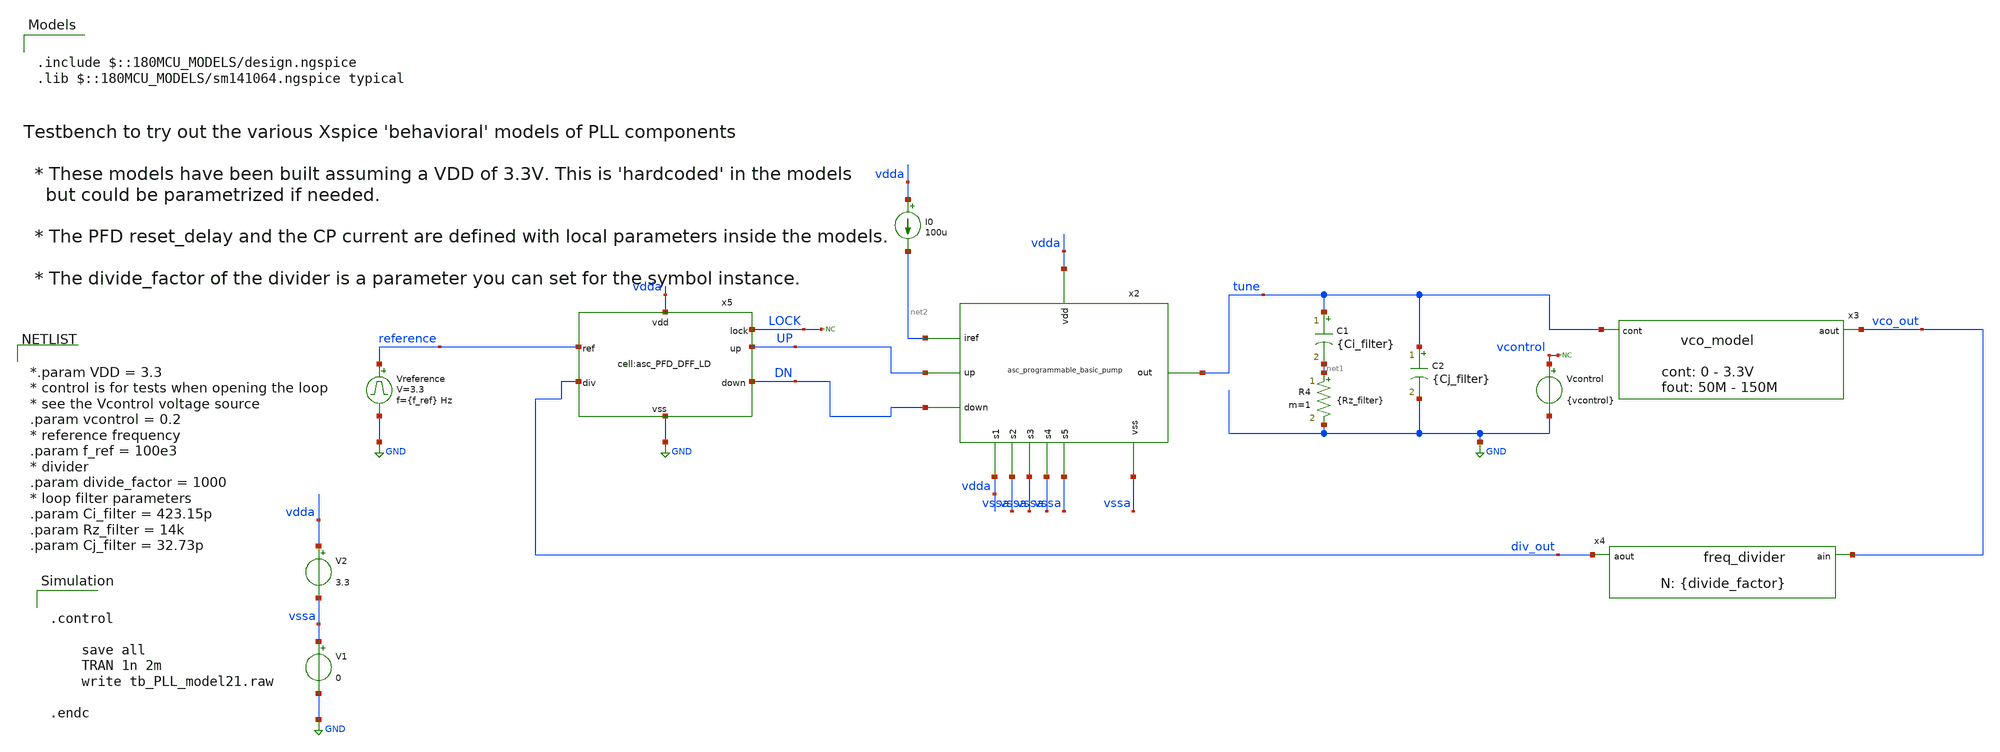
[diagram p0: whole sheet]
** sch_path: designs/libs/tb_pll/tb_PLL_PFD_CP_model_LD.sch
**.subckt tb_PLL_PFD_CP_model_LD
Vcontrol vcontrol GND {vcontrol}
Vreference reference GND pulse 0 3.3 '0.495/ {f_ref} ' '0.01/{f_ref} ' '0.01/{f_ref} ' '0.49/{f_ref} '
+ '1/{f_ref} '
C1 tune net1 {Ci_filter} m=1
R4 net1 GND {Rz_filter} m=1
* noconn vcontrol
C2 tune GND {Cj_filter} m=1
x3 vco_out tune vco_model
x4 div_out vco_out freq_divider divide_factor={divide_factor}
V1 vssa GND 0
V2 vdda vssa 3.3
I0 vdda net2 100u
x2 vdda tune vssa vssa vssa vssa vssa vdda DN UP net2 asc_programmable_basic_pump
x5 vdda LOCK GND div_out reference UP DN asc_PFD_DFF_LD
* noconn LOCK
**** begin user architecture code


.control

    save all
    TRAN 1n 2m
    write tb_PLL_model21.raw

.endc




*.param VDD = 3.3
* control is for tests when opening the loop
* see the Vcontrol voltage source
.param vcontrol = 0.2
* reference frequency
.param f_ref = 100e3
* divider
.param divide_factor = 1000
* loop filter parameters
.param Ci_filter = 423.15p
.param Rz_filter = 14k
.param Cj_filter = 32.73p



.include $::180MCU_MODELS/design.ngspice
.lib $::180MCU_MODELS/sm141064.ngspice typical

**** end user architecture code
**.ends
.GLOBAL GND
.end
